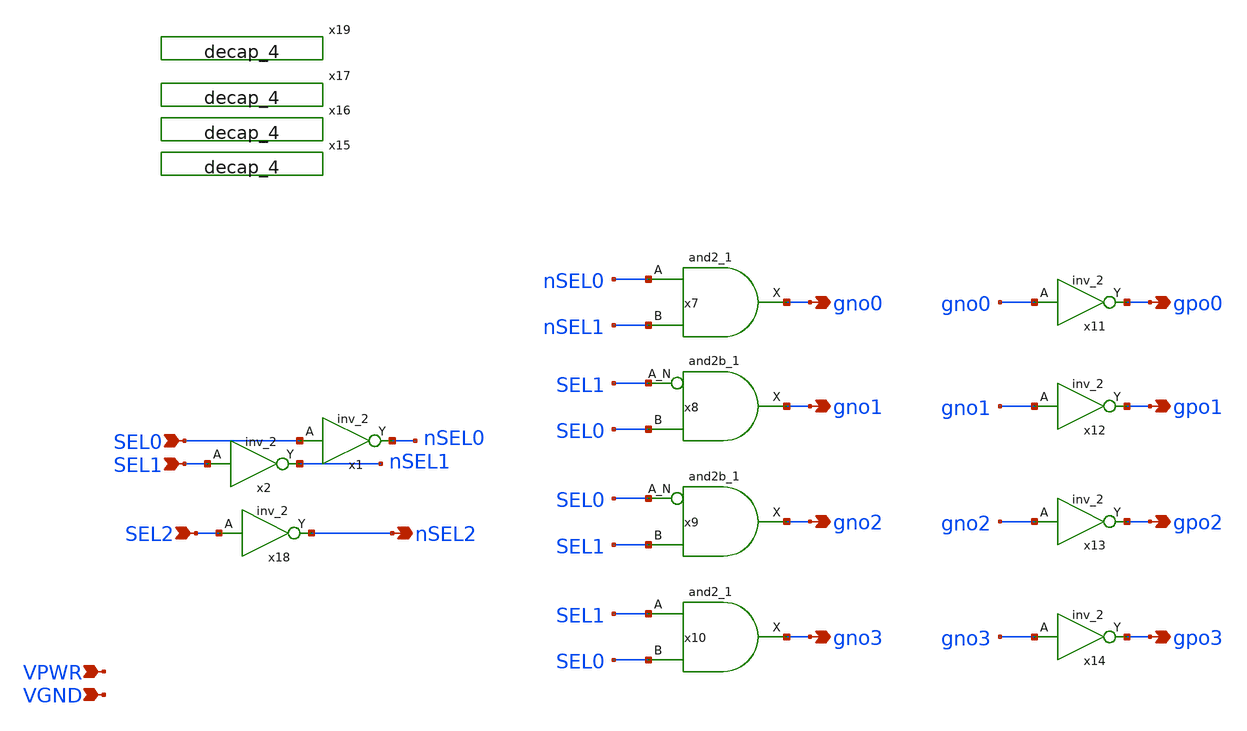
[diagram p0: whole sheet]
** sch_path: xschem/passgatesCtrlManual.sch
**.subckt passgatesCtrlManual SEL0 SEL1 SEL2 gno0 gpo0 gno1 gpo1 gno2 gpo2 gno3 gpo3 nSEL2 VPWR VGND
*.ipin SEL0
*.ipin SEL1
*.ipin SEL2
*.opin gno0
*.opin gpo0
*.opin gno1
*.opin gpo1
*.opin gno2
*.opin gpo2
*.opin gno3
*.opin gpo3
*.opin nSEL2
*.ipin VPWR
*.ipin VGND
x1 SEL0 VGND VGND VPWR VPWR nSEL0 sky130_fd_sc_hd__inv_2
x2 SEL1 VGND VGND VPWR VPWR nSEL1 sky130_fd_sc_hd__inv_2
x7 nSEL0 nSEL1 VGND VGND VPWR VPWR gno0 sky130_fd_sc_hd__and2_1
x10 SEL1 SEL0 VGND VGND VPWR VPWR gno3 sky130_fd_sc_hd__and2_1
x11 gno0 VGND VGND VPWR VPWR gpo0 sky130_fd_sc_hd__inv_2
x12 gno1 VGND VGND VPWR VPWR gpo1 sky130_fd_sc_hd__inv_2
x13 gno2 VGND VGND VPWR VPWR gpo2 sky130_fd_sc_hd__inv_2
x14 gno3 VGND VGND VPWR VPWR gpo3 sky130_fd_sc_hd__inv_2
x15 VGND VGND VPWR VPWR sky130_fd_sc_hd__decap_4
x16 VGND VGND VPWR VPWR sky130_fd_sc_hd__decap_4
x17 VGND VGND VPWR VPWR sky130_fd_sc_hd__decap_4
x8 SEL1 SEL0 VGND VGND VPWR VPWR gno1 sky130_fd_sc_hd__and2b_1
x9 SEL0 SEL1 VGND VGND VPWR VPWR gno2 sky130_fd_sc_hd__and2b_1
x18 SEL2 VGND VGND VPWR VPWR nSEL2 sky130_fd_sc_hd__inv_2
x19 VGND VGND VPWR VPWR sky130_fd_sc_hd__decap_4
**.ends
.end
